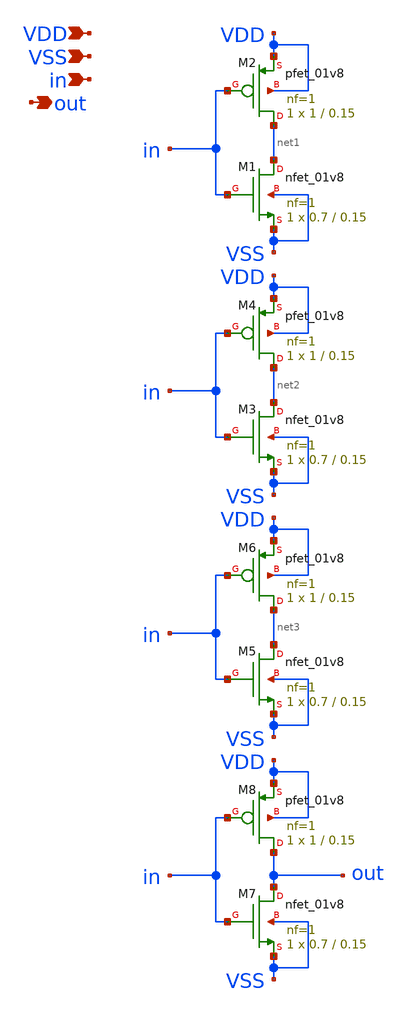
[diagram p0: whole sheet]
** sch_path: FO4/FO4.sch
**.subckt FO4 VDD VSS in out
*.ipin VDD
*.ipin VSS
*.ipin in
*.opin out
XM1 net1 in VSS VSS sky130_fd_pr__nfet_01v8 L=0.15 W=0.7 nf=1 ad='int((nf+1)/2) * W/nf * 0.29' as='int((nf+2)/2) * W/nf * 0.29'
+ pd='2*int((nf+1)/2) * (W/nf + 0.29)' ps='2*int((nf+2)/2) * (W/nf + 0.29)' nrd='0.29 / W' nrs='0.29 / W'
+ sa=0 sb=0 sd=0 mult=1 m=1
XM2 net1 in VDD VDD sky130_fd_pr__pfet_01v8 L=0.15 W=1 nf=1 ad='int((nf+1)/2) * W/nf * 0.29' as='int((nf+2)/2) * W/nf * 0.29'
+ pd='2*int((nf+1)/2) * (W/nf + 0.29)' ps='2*int((nf+2)/2) * (W/nf + 0.29)' nrd='0.29 / W' nrs='0.29 / W'
+ sa=0 sb=0 sd=0 mult=1 m=1
XM3 net2 in VSS VSS sky130_fd_pr__nfet_01v8 L=0.15 W=0.7 nf=1 ad='int((nf+1)/2) * W/nf * 0.29' as='int((nf+2)/2) * W/nf * 0.29'
+ pd='2*int((nf+1)/2) * (W/nf + 0.29)' ps='2*int((nf+2)/2) * (W/nf + 0.29)' nrd='0.29 / W' nrs='0.29 / W'
+ sa=0 sb=0 sd=0 mult=1 m=1
XM4 net2 in VDD VDD sky130_fd_pr__pfet_01v8 L=0.15 W=1 nf=1 ad='int((nf+1)/2) * W/nf * 0.29' as='int((nf+2)/2) * W/nf * 0.29'
+ pd='2*int((nf+1)/2) * (W/nf + 0.29)' ps='2*int((nf+2)/2) * (W/nf + 0.29)' nrd='0.29 / W' nrs='0.29 / W'
+ sa=0 sb=0 sd=0 mult=1 m=1
XM5 net3 in VSS VSS sky130_fd_pr__nfet_01v8 L=0.15 W=0.7 nf=1 ad='int((nf+1)/2) * W/nf * 0.29' as='int((nf+2)/2) * W/nf * 0.29'
+ pd='2*int((nf+1)/2) * (W/nf + 0.29)' ps='2*int((nf+2)/2) * (W/nf + 0.29)' nrd='0.29 / W' nrs='0.29 / W'
+ sa=0 sb=0 sd=0 mult=1 m=1
XM6 net3 in VDD VDD sky130_fd_pr__pfet_01v8 L=0.15 W=1 nf=1 ad='int((nf+1)/2) * W/nf * 0.29' as='int((nf+2)/2) * W/nf * 0.29'
+ pd='2*int((nf+1)/2) * (W/nf + 0.29)' ps='2*int((nf+2)/2) * (W/nf + 0.29)' nrd='0.29 / W' nrs='0.29 / W'
+ sa=0 sb=0 sd=0 mult=1 m=1
XM7 out in VSS VSS sky130_fd_pr__nfet_01v8 L=0.15 W=0.7 nf=1 ad='int((nf+1)/2) * W/nf * 0.29' as='int((nf+2)/2) * W/nf * 0.29'
+ pd='2*int((nf+1)/2) * (W/nf + 0.29)' ps='2*int((nf+2)/2) * (W/nf + 0.29)' nrd='0.29 / W' nrs='0.29 / W'
+ sa=0 sb=0 sd=0 mult=1 m=1
XM8 out in VDD VDD sky130_fd_pr__pfet_01v8 L=0.15 W=1 nf=1 ad='int((nf+1)/2) * W/nf * 0.29' as='int((nf+2)/2) * W/nf * 0.29'
+ pd='2*int((nf+1)/2) * (W/nf + 0.29)' ps='2*int((nf+2)/2) * (W/nf + 0.29)' nrd='0.29 / W' nrs='0.29 / W'
+ sa=0 sb=0 sd=0 mult=1 m=1
**.ends
.end
